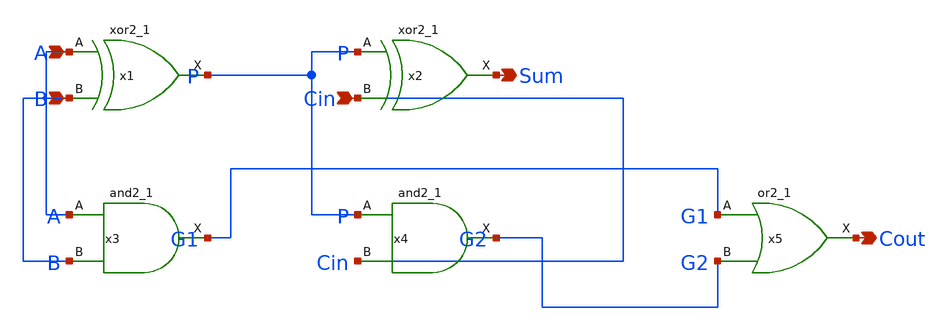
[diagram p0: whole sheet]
** sch_path: xschem/full_adder_clean.sch
**.subckt full_adder_clean A B Cin Sum Cout
*.ipin A
*.ipin B
*.ipin Cin
*.opin Sum
*.opin Cout
x1 A B VGND VNB VPB VPWR P sky130_fd_sc_hd__xor2_1
x2 P Cin VGND VNB VPB VPWR Sum sky130_fd_sc_hd__xor2_1
x3 A B VGND VNB VPB VPWR G1 sky130_fd_sc_hd__and2_1
x4 P Cin VGND VNB VPB VPWR G2 sky130_fd_sc_hd__and2_1
x5 G1 G2 VGND VNB VPB VPWR Cout sky130_fd_sc_hd__or2_1
**.ends
.end
